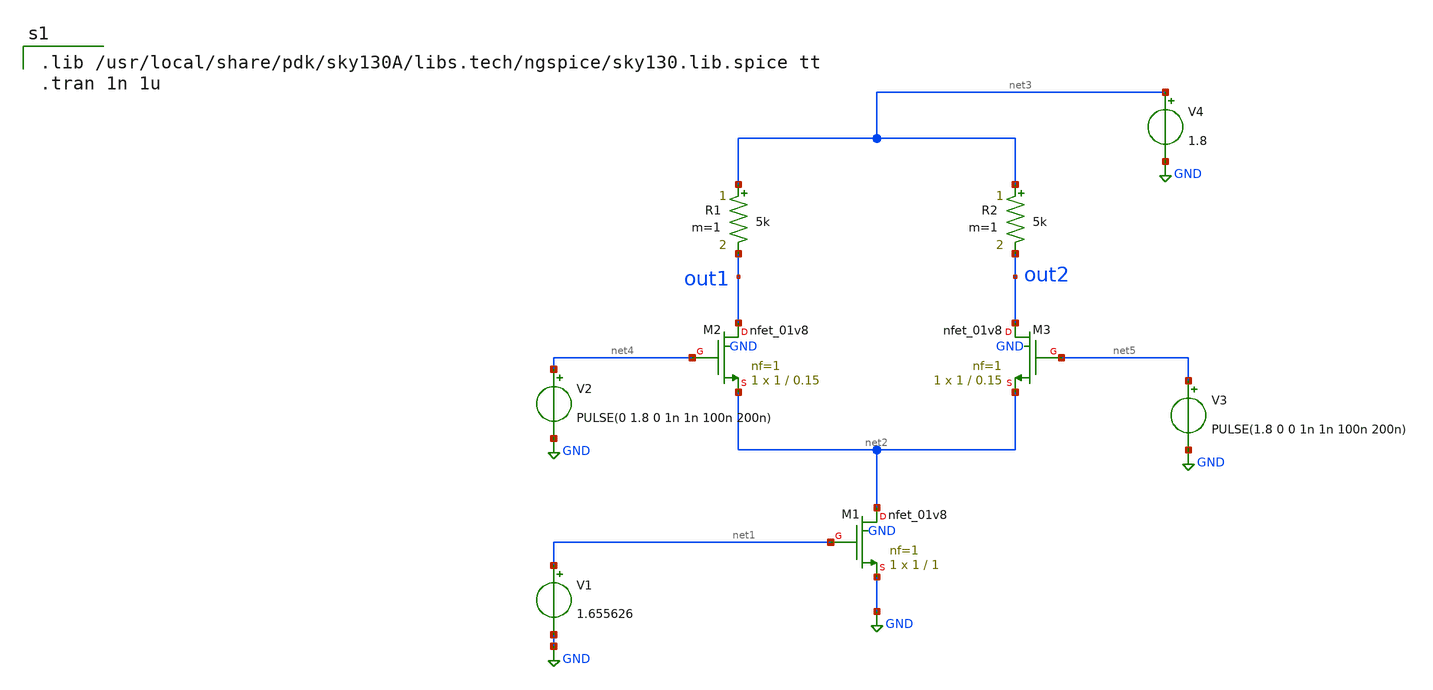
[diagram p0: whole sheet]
** sch_path: Current Steering Cell/Current_Steering_Cell.sch
**.subckt Current_Steering_Cell
XM1 net2 net1 GND GND sky130_fd_pr__nfet_01v8 L=1 W=1 nf=1 ad='int((1 + 1)/2) * 1 / 1 * 0.29' as='int((1 + 2)/2) * 1 / 1 * 0.29'
+ pd='2*int((1 + 1)/2) * (1 / 1 + 0.29)' ps='2*int((1 + 2)/2) * (1 / 1 + 0.29)' nrd='0.29 / 1 ' nrs='0.29 / 1 '
+ sa=0 sb=0 sd=0 mult=1 m=1
V1 net1 GND 1.655626
XM2 out1 net4 net2 GND sky130_fd_pr__nfet_01v8 L=0.15 W=1 nf=1 ad='int((1 + 1)/2) * 1 / 1 * 0.29' as='int((1 + 2)/2) * 1 / 1 * 0.29'
+ pd='2*int((1 + 1)/2) * (1 / 1 + 0.29)' ps='2*int((1 + 2)/2) * (1 / 1 + 0.29)' nrd='0.29 / 1 ' nrs='0.29 / 1 '
+ sa=0 sb=0 sd=0 mult=1 m=1
XM3 out2 net5 net2 GND sky130_fd_pr__nfet_01v8 L=0.15 W=1 nf=1 ad='int((1 + 1)/2) * 1 / 1 * 0.29' as='int((1 + 2)/2) * 1 / 1 * 0.29'
+ pd='2*int((1 + 1)/2) * (1 / 1 + 0.29)' ps='2*int((1 + 2)/2) * (1 / 1 + 0.29)' nrd='0.29 / 1 ' nrs='0.29 / 1 '
+ sa=0 sb=0 sd=0 mult=1 m=1
R1 net3 out1 5k m=1
R2 net3 out2 5k m=1
V2 net4 GND PULSE(0 1.8 0 1n 1n 100n 200n)
V3 net5 GND PULSE(1.8 0 0 1n 1n 100n 200n)
V4 net3 GND 1.8
**** begin user architecture code

.lib /usr/local/share/pdk/sky130A/libs.tech/ngspice/sky130.lib.spice tt
.tran 1n 1u

**** end user architecture code
**.ends
.GLOBAL GND
.end
